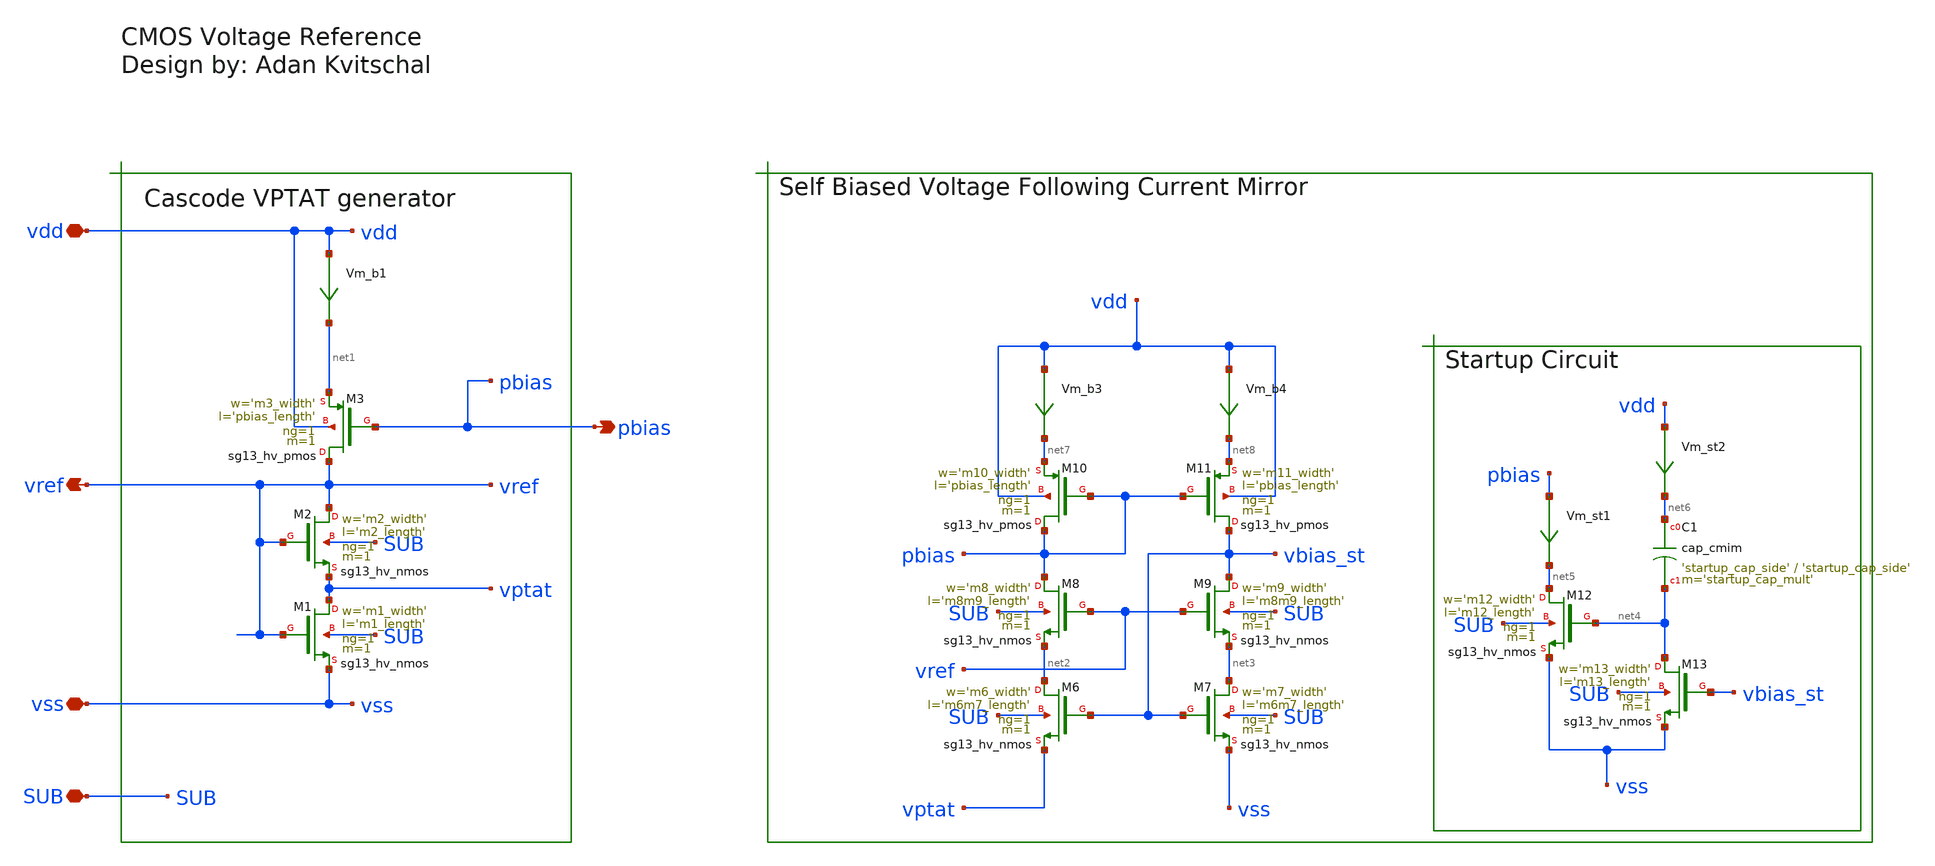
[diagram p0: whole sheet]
** sch_path: sch/cmos_vref/cmos_vref_default.sch
**.subckt cmos_vref_default vss SUB vdd pbias vref
*.iopin vss
*.iopin SUB
*.iopin vdd
*.opin pbias
*.opin vref
Vm_b1 vdd net1 0
.save i(vm_b1)
XM1 vptat vref vss SUB sg13_hv_nmos w='m1_width' l='m1_length' ng=1 m=1 mm_ok=1
XM2 vref vref vptat SUB sg13_hv_nmos w='m2_width' l='m2_length' ng=1 m=1 mm_ok=1
XM3 vref pbias net1 vdd sg13_hv_pmos w='m3_width' l='pbias_length' ng=1 m=1 mm_ok=1
Vm_st1 pbias net5 0
.save i(vm_st1)
Vm_st2 vdd net6 0
.save i(vm_st2)
Vm_b3 vdd net7 0
.save i(vm_b3)
Vm_b4 vdd net8 0
.save i(vm_b4)
XM7 net3 vbias_st vss SUB sg13_hv_nmos w='m7_width' l='m6m7_length' ng=1 m=1 mm_ok=1
XM11 vbias_st pbias net8 vdd sg13_hv_pmos w='m11_width' l='pbias_length' ng=1 m=1 mm_ok=1
XM6 net2 vbias_st vptat SUB sg13_hv_nmos w='m6_width' l='m6m7_length' ng=1 m=1 mm_ok=1
XM9 vbias_st vref net3 SUB sg13_hv_nmos w='m9_width' l='m8m9_length' ng=1 m=1 mm_ok=1
XM8 pbias vref net2 SUB sg13_hv_nmos w='m8_width' l='m8m9_length' ng=1 m=1 mm_ok=1
XM10 pbias pbias net7 vdd sg13_hv_pmos w='m10_width' l='pbias_length' ng=1 m=1 mm_ok=1
XM13 net4 vbias_st vss SUB sg13_hv_nmos w='m13_width' l='m13_length' ng=1 m=1 mm_ok=1
XM12 net5 net4 vss SUB sg13_hv_nmos w='m12_width' l='m12_length' ng=1 m=1 mm_ok=1
XC1 net6 net4 cap_cmim w='startup_cap_side' l='startup_cap_side' m='startup_cap_mult' mm_ok=1
**.ends
.end
